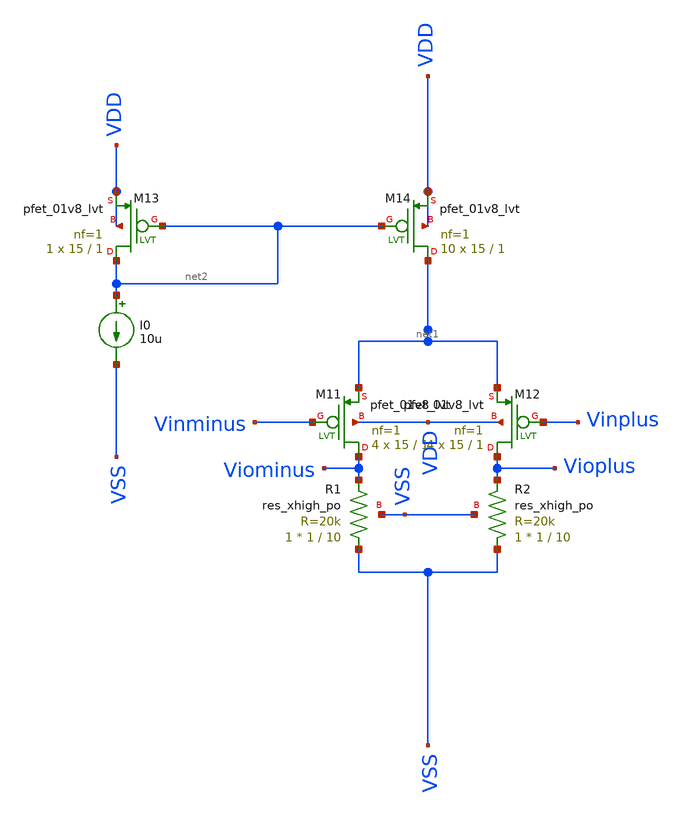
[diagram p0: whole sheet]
** sch_path: userLib/Preamp.sch
**.subckt Preamp
XR1 VSS Viominus VSS sky130_fd_pr__res_xhigh_po W=1 L=10 mult=1 m=1
XR2 VSS Vioplus VSS sky130_fd_pr__res_xhigh_po W=1 L=10 mult=1 m=1
I0 net2 VSS 10u
XM11 Viominus Vinminus net1 VDD sky130_fd_pr__pfet_01v8_lvt L=1 W=15 nf=1 ad='int((nf+1)/2) * W/nf * 0.29'
+ as='int((nf+2)/2) * W/nf * 0.29' pd='2*int((nf+1)/2) * (W/nf + 0.29)' ps='2*int((nf+2)/2) * (W/nf + 0.29)'
+ nrd='0.29 / W' nrs='0.29 / W' sa=0 sb=0 sd=0 mult=4 m=4
XM12 Vioplus Vinplus net1 VDD sky130_fd_pr__pfet_01v8_lvt L=1 W=15 nf=1 ad='int((nf+1)/2) * W/nf * 0.29'
+ as='int((nf+2)/2) * W/nf * 0.29' pd='2*int((nf+1)/2) * (W/nf + 0.29)' ps='2*int((nf+2)/2) * (W/nf + 0.29)'
+ nrd='0.29 / W' nrs='0.29 / W' sa=0 sb=0 sd=0 mult=4 m=4
XM13 net2 net2 VDD VDD sky130_fd_pr__pfet_01v8_lvt L=1 W=15 nf=1 ad='int((nf+1)/2) * W/nf * 0.29' as='int((nf+2)/2) * W/nf * 0.29'
+ pd='2*int((nf+1)/2) * (W/nf + 0.29)' ps='2*int((nf+2)/2) * (W/nf + 0.29)' nrd='0.29 / W' nrs='0.29 / W'
+ sa=0 sb=0 sd=0 mult=1 m=1
XM14 net1 net2 VDD VDD sky130_fd_pr__pfet_01v8_lvt L=1 W=15 nf=1 ad='int((nf+1)/2) * W/nf * 0.29' as='int((nf+2)/2) * W/nf * 0.29'
+ pd='2*int((nf+1)/2) * (W/nf + 0.29)' ps='2*int((nf+2)/2) * (W/nf + 0.29)' nrd='0.29 / W' nrs='0.29 / W'
+ sa=0 sb=0 sd=0 mult=10 m=10
**.ends
.end
